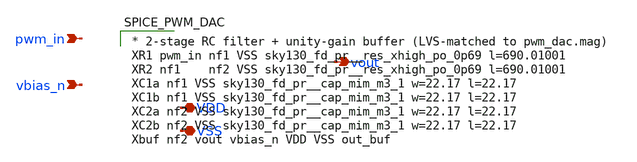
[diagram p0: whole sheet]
** sch_path: bvm_analog_tapeout/analog/pwm_dac/xschem/pwm_dac.sch
**.subckt pwm_dac pwm_in vout vbias_n VDD VSS
*.ipin pwm_in
*.opin vout
*.ipin vbias_n
*.iopin VDD
*.iopin VSS
**** begin user architecture code

* 2-stage RC filter + unity-gain buffer (LVS-matched to pwm_dac.mag)
XR1 pwm_in nf1 VSS sky130_fd_pr__res_xhigh_po_0p69 l=690.01001
XR2 nf1    nf2 VSS sky130_fd_pr__res_xhigh_po_0p69 l=690.01001
XC1a nf1 VSS sky130_fd_pr__cap_mim_m3_1 w=22.17 l=22.17
XC1b nf1 VSS sky130_fd_pr__cap_mim_m3_1 w=22.17 l=22.17
XC2a nf2 VSS sky130_fd_pr__cap_mim_m3_1 w=22.17 l=22.17
XC2b nf2 VSS sky130_fd_pr__cap_mim_m3_1 w=22.17 l=22.17
Xbuf nf2 vout vbias_n VDD VSS out_buf

**** end user architecture code
**.ends
.end
